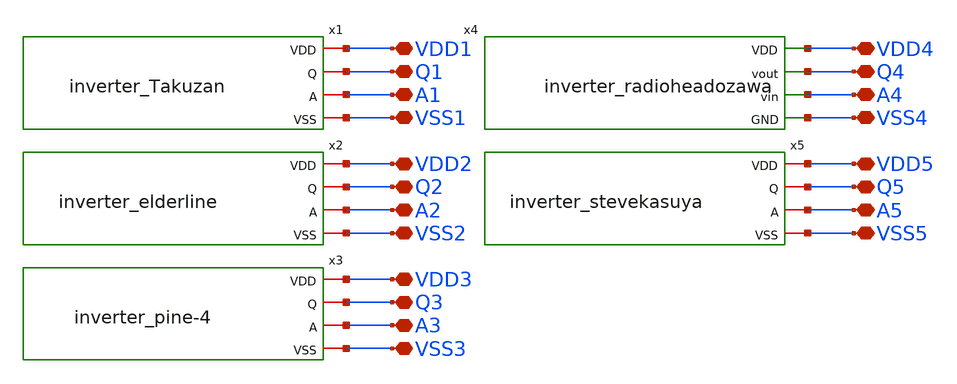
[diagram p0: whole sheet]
** sch_path: Submitted/all_member_inverter.sch
**.subckt all_member_inverter VDD1 Q1 A1 VSS1 VDD2 Q2 A2 VSS2 VDD3 Q3 A3 VSS3 VDD4 Q4 A4 VSS4 VDD5
*+ Q5 A5 VSS5
*.iopin VDD1
*.iopin Q1
*.iopin A1
*.iopin VSS1
*.iopin VDD2
*.iopin Q2
*.iopin A2
*.iopin VSS2
*.iopin VDD3
*.iopin Q3
*.iopin A3
*.iopin VSS3
*.iopin VDD4
*.iopin Q4
*.iopin A4
*.iopin VSS4
*.iopin VDD5
*.iopin Q5
*.iopin A5
*.iopin VSS5
x1 VDD1 Q1 A1 VSS1 inverter_Takuzan
x2 VDD2 Q2 A2 VSS2 inverter_elderline
x3 VDD3 Q3 A3 VSS3 inverter_pine-4
x4 VDD4 Q4 A4 VSS4 inverter_radioheadozawa
x5 VDD5 Q5 A5 VSS5 inverter_stevekasuya
**.ends
.end
